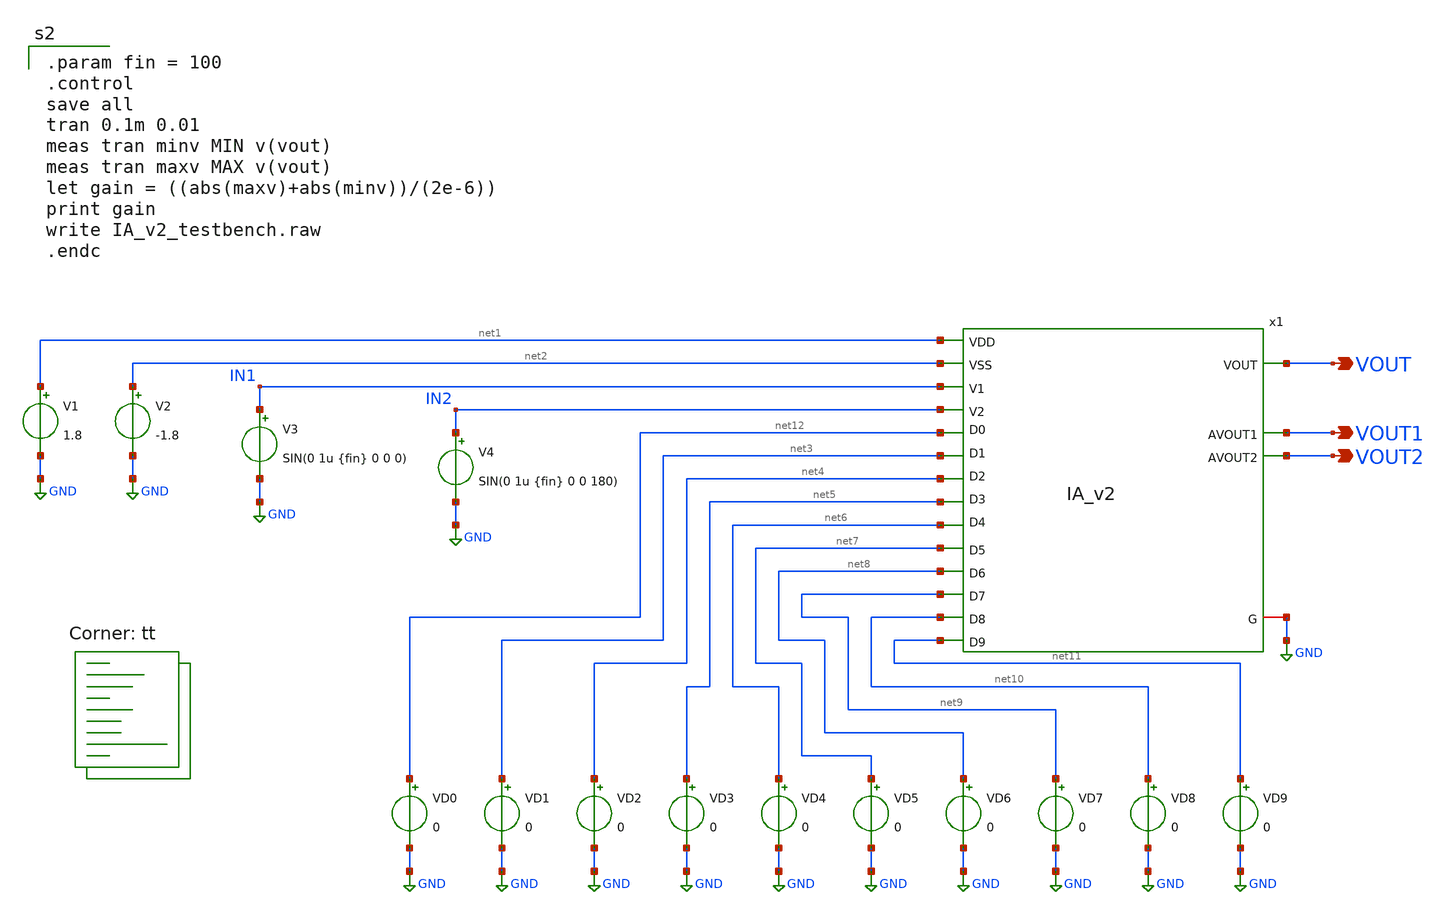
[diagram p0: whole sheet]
** sch_path: xschem/IA_v2_testbench.sch
**.subckt IA_v2_testbench VOUT VOUT1 VOUT2
*.opin VOUT
*.opin VOUT1
*.opin VOUT2
V1 net1 GND 1.8
V2 net2 GND -1.8
V3 IN1 GND SIN(0 1u {fin} 0 0 0)
V4 IN2 GND SIN(0 1u {fin} 0 0 180)
VD0 net12 GND 0
VD1 net3 GND 0
VD2 net4 GND 0
VD3 net5 GND 0
VD4 net6 GND 0
VD5 net7 GND 0
VD6 net8 GND 0
VD7 net9 GND 0
VD8 net10 GND 0
VD9 net11 GND 0
x1 VOUT1 net1 net2 VOUT IN1 IN2 VOUT2 net6 net5 net4 net3 net12 GND net8 net9 net10 net7 net11 IA_v2
**** begin user architecture code

.param fin = 100
.control
save all
tran 0.1m 0.01
meas tran minv MIN v(vout)
meas tran maxv MAX v(vout)
let gain = ((abs(maxv)+abs(minv))/(2e-6))
print gain
write IA_v2_testbench.raw
.endc

.lib $::SKYWATER_MODELS/sky130.lib.spice tt
**** end user architecture code
**.ends

* expanding   symbol:  /home/caonam/OpenLane/FINALPROJECT/sky130_hcmus_ip__instramp/xschem/IA_v2.sym
*+ # of pins=18
** sym_path: /home/caonam/OpenLane/FINALPROJECT/sky130_hcmus_ip__instramp/xschem/IA_v2.sym
** sch_path: /home/caonam/OpenLane/FINALPROJECT/sky130_hcmus_ip__instramp/xschem/IA_v2.sch
.subckt IA_v2 AVOUT1 VDD VSS VOUT V1 V2 AVOUT2 D4 D3 D2 D1 D0 G D6 D7 D8 D5 D9
*.opin VOUT
*.iopin G
*.ipin VDD
*.ipin VSS
*.ipin V1
*.ipin V2
*.ipin D4
*.ipin D3
*.ipin D2
*.ipin D1
*.ipin D0
*.ipin D9
*.ipin D8
*.ipin D7
*.ipin D6
*.ipin D5
*.opin AVOUT1
*.opin AVOUT2
x4 VDD VSS V2 net3 AVOUT1 opamp
x5 VDD VSS V1 net4 AVOUT2 opamp
x6 VDD VSS net2 net1 VOUT opamp
x1 G net3 AVOUT1 D0 D1 D2 D3 D4 RA_array
x2 G net4 AVOUT2 D0 D1 D2 D3 D4 RA_array
x3 G net1 VOUT D5 D6 D7 D8 D9 RA_array
x7 G net2 G D5 D6 D7 D8 D9 RA_array
XR4 net5 net1 G sky130_fd_pr__res_high_po_0p69 L=127.08 mult=64 m=64
XR1 net3 net4 G sky130_fd_pr__res_high_po_0p69 L=127.08 mult=64 m=64
XR2 net2 net6 G sky130_fd_pr__res_high_po_0p69 L=127.08 mult=64 m=64
x8 VDD VSS AVOUT1 net5 net5 opamp
x9 VDD VSS AVOUT2 net6 net6 opamp
.ends


* expanding   symbol:  ../xschem/opamp.sym # of pins=5
** sym_path: xschem/opamp.sym
** sch_path: xschem/opamp.sch
.subckt opamp VDD VSS V1 V2 VOUT
*.ipin VSS
*.ipin VDD
*.ipin V2
*.ipin V1
*.opin VOUT
XM2 net5 V2 net1 VSS sky130_fd_pr__nfet_01v8 L=1 W=8.5 nf=1 ad='int((nf+1)/2) * W/nf * 0.29' as='int((nf+2)/2) * W/nf * 0.29'
+ pd='2*int((nf+1)/2) * (W/nf + 0.29)' ps='2*int((nf+2)/2) * (W/nf + 0.29)' nrd='0.29 / W' nrs='0.29 / W'
+ sa=0 sb=0 sd=0 mult=1 m=1
XM1 net6 net5 VDD VDD sky130_fd_pr__pfet_01v8 L=1 W=41 nf=1 ad='int((nf+1)/2) * W/nf * 0.29' as='int((nf+2)/2) * W/nf * 0.29'
+ pd='2*int((nf+1)/2) * (W/nf + 0.29)' ps='2*int((nf+2)/2) * (W/nf + 0.29)' nrd='0.29 / W' nrs='0.29 / W'
+ sa=0 sb=0 sd=0 mult=1 m=1
XM4 net6 V1 net1 VSS sky130_fd_pr__nfet_01v8 L=1 W=8.5 nf=1 ad='int((nf+1)/2) * W/nf * 0.29' as='int((nf+2)/2) * W/nf * 0.29'
+ pd='2*int((nf+1)/2) * (W/nf + 0.29)' ps='2*int((nf+2)/2) * (W/nf + 0.29)' nrd='0.29 / W' nrs='0.29 / W'
+ sa=0 sb=0 sd=0 mult=1 m=1
XM5 net1 net4 VSS VSS sky130_fd_pr__nfet_01v8 L=1 W=20 nf=1 ad='int((nf+1)/2) * W/nf * 0.29' as='int((nf+2)/2) * W/nf * 0.29'
+ pd='2*int((nf+1)/2) * (W/nf + 0.29)' ps='2*int((nf+2)/2) * (W/nf + 0.29)' nrd='0.29 / W' nrs='0.29 / W'
+ sa=0 sb=0 sd=0 mult=1 m=1
XM6 VOUT net4 VSS VSS sky130_fd_pr__nfet_01v8 L=1 W=19 nf=1 ad='int((nf+1)/2) * W/nf * 0.29' as='int((nf+2)/2) * W/nf * 0.29'
+ pd='2*int((nf+1)/2) * (W/nf + 0.29)' ps='2*int((nf+2)/2) * (W/nf + 0.29)' nrd='0.29 / W' nrs='0.29 / W'
+ sa=0 sb=0 sd=0 mult=1 m=1
XM7 net4 net4 VSS VSS sky130_fd_pr__nfet_01v8 L=1 W=20 nf=1 ad='int((nf+1)/2) * W/nf * 0.29' as='int((nf+2)/2) * W/nf * 0.29'
+ pd='2*int((nf+1)/2) * (W/nf + 0.29)' ps='2*int((nf+2)/2) * (W/nf + 0.29)' nrd='0.29 / W' nrs='0.29 / W'
+ sa=0 sb=0 sd=0 mult=1 m=1
XM3 net5 net5 VDD VDD sky130_fd_pr__pfet_01v8 L=1 W=41 nf=1 ad='int((nf+1)/2) * W/nf * 0.29' as='int((nf+2)/2) * W/nf * 0.29'
+ pd='2*int((nf+1)/2) * (W/nf + 0.29)' ps='2*int((nf+2)/2) * (W/nf + 0.29)' nrd='0.29 / W' nrs='0.29 / W'
+ sa=0 sb=0 sd=0 mult=1 m=1
XM8 VOUT net6 VDD VDD sky130_fd_pr__pfet_01v8 L=1 W=40 nf=1 ad='int((nf+1)/2) * W/nf * 0.29' as='int((nf+2)/2) * W/nf * 0.29'
+ pd='2*int((nf+1)/2) * (W/nf + 0.29)' ps='2*int((nf+2)/2) * (W/nf + 0.29)' nrd='0.29 / W' nrs='0.29 / W'
+ sa=0 sb=0 sd=0 mult=2 m=2
XR3 net2 VDD VSS sky130_fd_pr__res_high_po W=1 L=50 mult=1 m=1
XR1 net3 net2 VSS sky130_fd_pr__res_high_po W=1 L=50 mult=1 m=1
XR2 net4 net3 VSS sky130_fd_pr__res_high_po W=1 L=50 mult=1 m=1
XR4 net7 VOUT VSS sky130_fd_pr__res_high_po W=1 L=7 mult=1 m=1
XC1 net7 net6 sky130_fd_pr__cap_mim_m3_1 W=5.55 L=10 MF=20 m=20
.ends


* expanding   symbol:  ../xschem/RA_array.sym # of pins=8
** sym_path: xschem/RA_array.sym
** sch_path: xschem/RA_array.sch
.subckt RA_array VSS R1 R2 D0 D1 D2 D3 D4
*.ipin VSS
*.iopin R2
*.ipin D0
*.ipin D1
*.ipin D2
*.ipin D3
*.ipin D4
*.iopin R1
XR1 net1 R2 VSS sky130_fd_pr__res_xhigh_po W=2 L=4 mult=1 m=1
XR4 net3 R2 VSS sky130_fd_pr__res_xhigh_po W=2 L=16 mult=1 m=1
XR5 net4 R2 VSS sky130_fd_pr__res_xhigh_po W=2 L=32 mult=1 m=1
XR6 net5 R2 VSS sky130_fd_pr__res_xhigh_po W=2 L=64 mult=1 m=1
XR7 R1 R2 VSS sky130_fd_pr__res_xhigh_po W=2 L=64 mult=1 m=1
XM2 net5 D0 R1 VSS sky130_fd_pr__nfet_g5v0d10v5 L=0.5 W=5 nf=1 ad='int((nf+1)/2) * W/nf * 0.29' as='int((nf+2)/2) * W/nf * 0.29'
+ pd='2*int((nf+1)/2) * (W/nf + 0.29)' ps='2*int((nf+2)/2) * (W/nf + 0.29)' nrd='0.29 / W' nrs='0.29 / W'
+ sa=0 sb=0 sd=0 mult=1 m=1
XM3 net4 D1 R1 VSS sky130_fd_pr__nfet_g5v0d10v5 L=0.5 W=5 nf=1 ad='int((nf+1)/2) * W/nf * 0.29' as='int((nf+2)/2) * W/nf * 0.29'
+ pd='2*int((nf+1)/2) * (W/nf + 0.29)' ps='2*int((nf+2)/2) * (W/nf + 0.29)' nrd='0.29 / W' nrs='0.29 / W'
+ sa=0 sb=0 sd=0 mult=1 m=1
XM4 net3 D2 R1 VSS sky130_fd_pr__nfet_g5v0d10v5 L=0.5 W=5 nf=1 ad='int((nf+1)/2) * W/nf * 0.29' as='int((nf+2)/2) * W/nf * 0.29'
+ pd='2*int((nf+1)/2) * (W/nf + 0.29)' ps='2*int((nf+2)/2) * (W/nf + 0.29)' nrd='0.29 / W' nrs='0.29 / W'
+ sa=0 sb=0 sd=0 mult=1 m=1
XM5 net2 D3 R1 VSS sky130_fd_pr__nfet_g5v0d10v5 L=0.5 W=5 nf=1 ad='int((nf+1)/2) * W/nf * 0.29' as='int((nf+2)/2) * W/nf * 0.29'
+ pd='2*int((nf+1)/2) * (W/nf + 0.29)' ps='2*int((nf+2)/2) * (W/nf + 0.29)' nrd='0.29 / W' nrs='0.29 / W'
+ sa=0 sb=0 sd=0 mult=1 m=1
XM6 net1 D4 R1 VSS sky130_fd_pr__nfet_g5v0d10v5 L=0.5 W=5 nf=1 ad='int((nf+1)/2) * W/nf * 0.29' as='int((nf+2)/2) * W/nf * 0.29'
+ pd='2*int((nf+1)/2) * (W/nf + 0.29)' ps='2*int((nf+2)/2) * (W/nf + 0.29)' nrd='0.29 / W' nrs='0.29 / W'
+ sa=0 sb=0 sd=0 mult=1 m=1
XR2 net2 R2 VSS sky130_fd_pr__res_xhigh_po W=2 L=8 mult=1 m=1
.ends

.GLOBAL GND
.end
